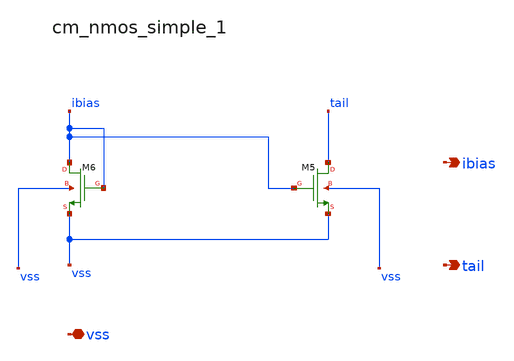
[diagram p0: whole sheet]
** sch_path: analog-db/raw/amp_018_telescopic_cascode/hier/blocks/cm_nmos_simple_1.sch
**.subckt cm_nmos_simple_1 vss ibias tail
*.iopin vss
*.opin ibias
*.opin tail
XM5 tail ibias vss vss sg13_lv_nmos w=x_dut_xm5_w l=x_dut_xm5_l ng=x_dut_xm5_ng m=x_dut_xm5_m
XM6 ibias ibias vss vss sg13_lv_nmos w=x_dut_xm6_w l=x_dut_xm6_l ng=1 m=x_dut_xm6_m
**.ends
.end
